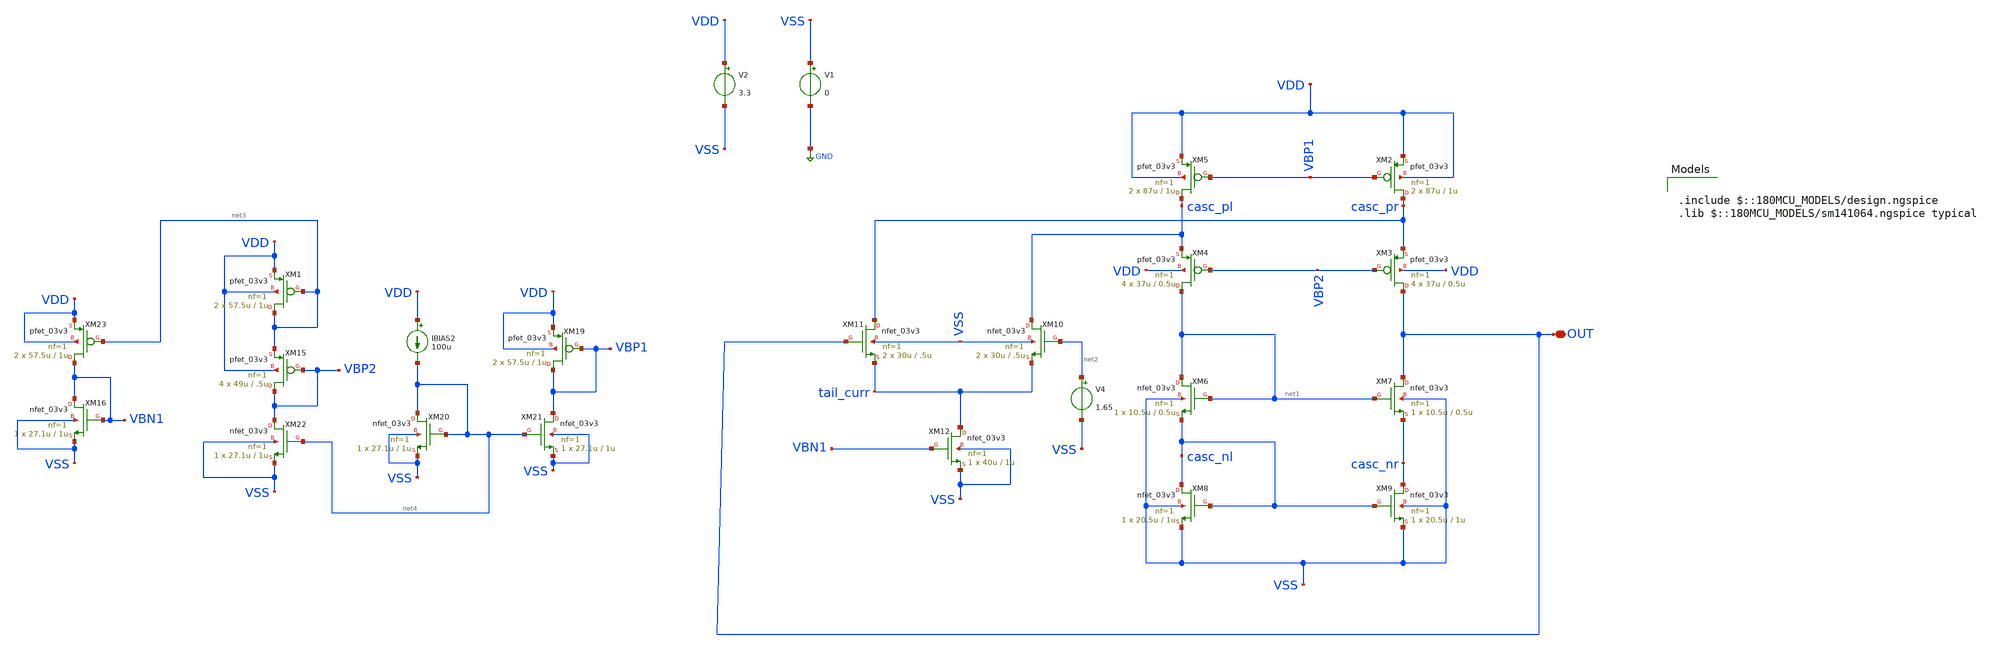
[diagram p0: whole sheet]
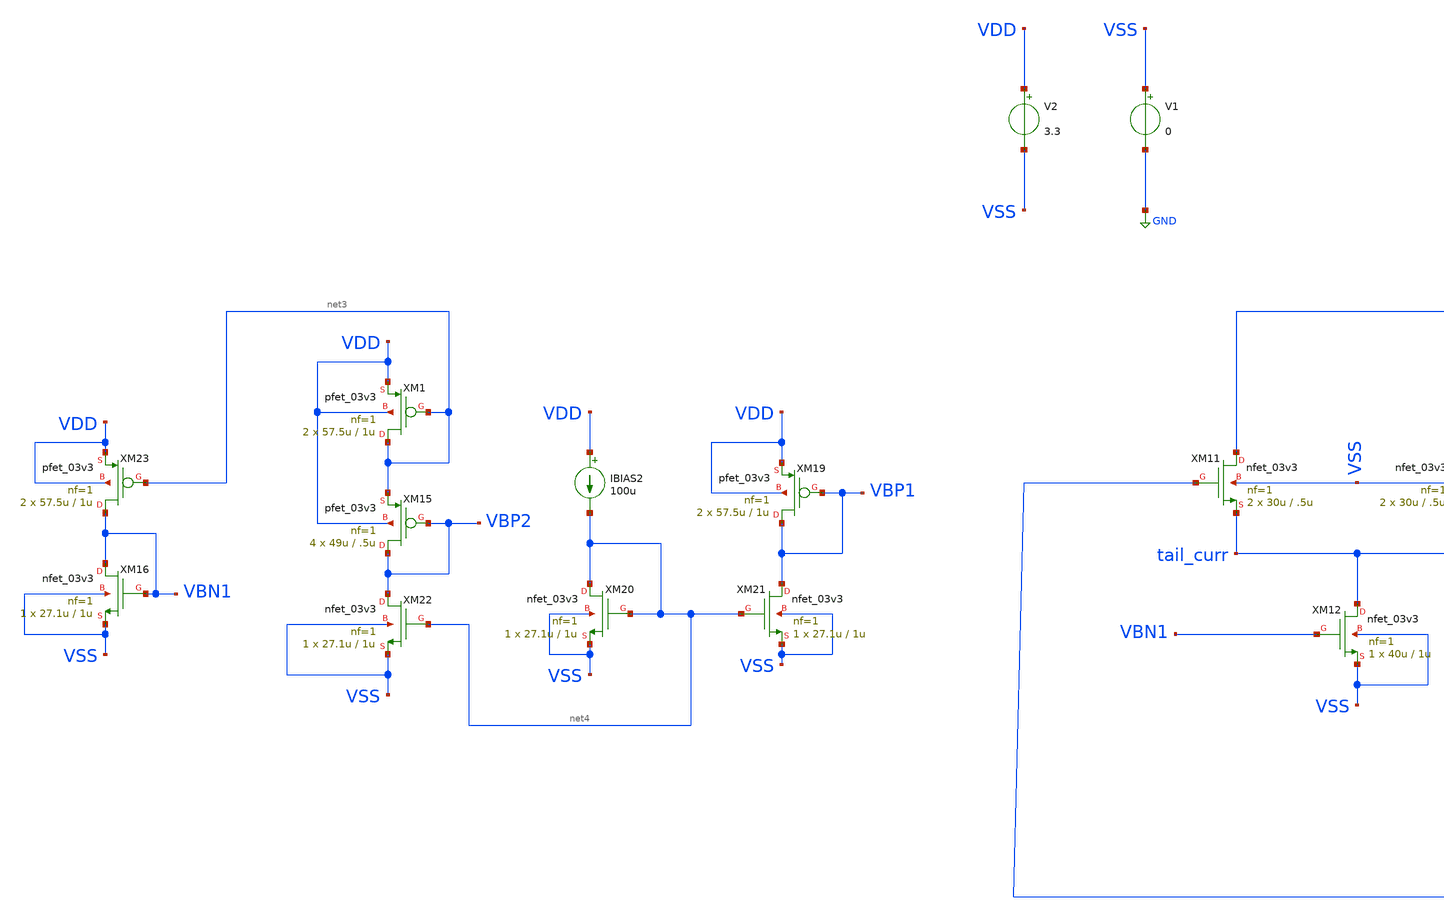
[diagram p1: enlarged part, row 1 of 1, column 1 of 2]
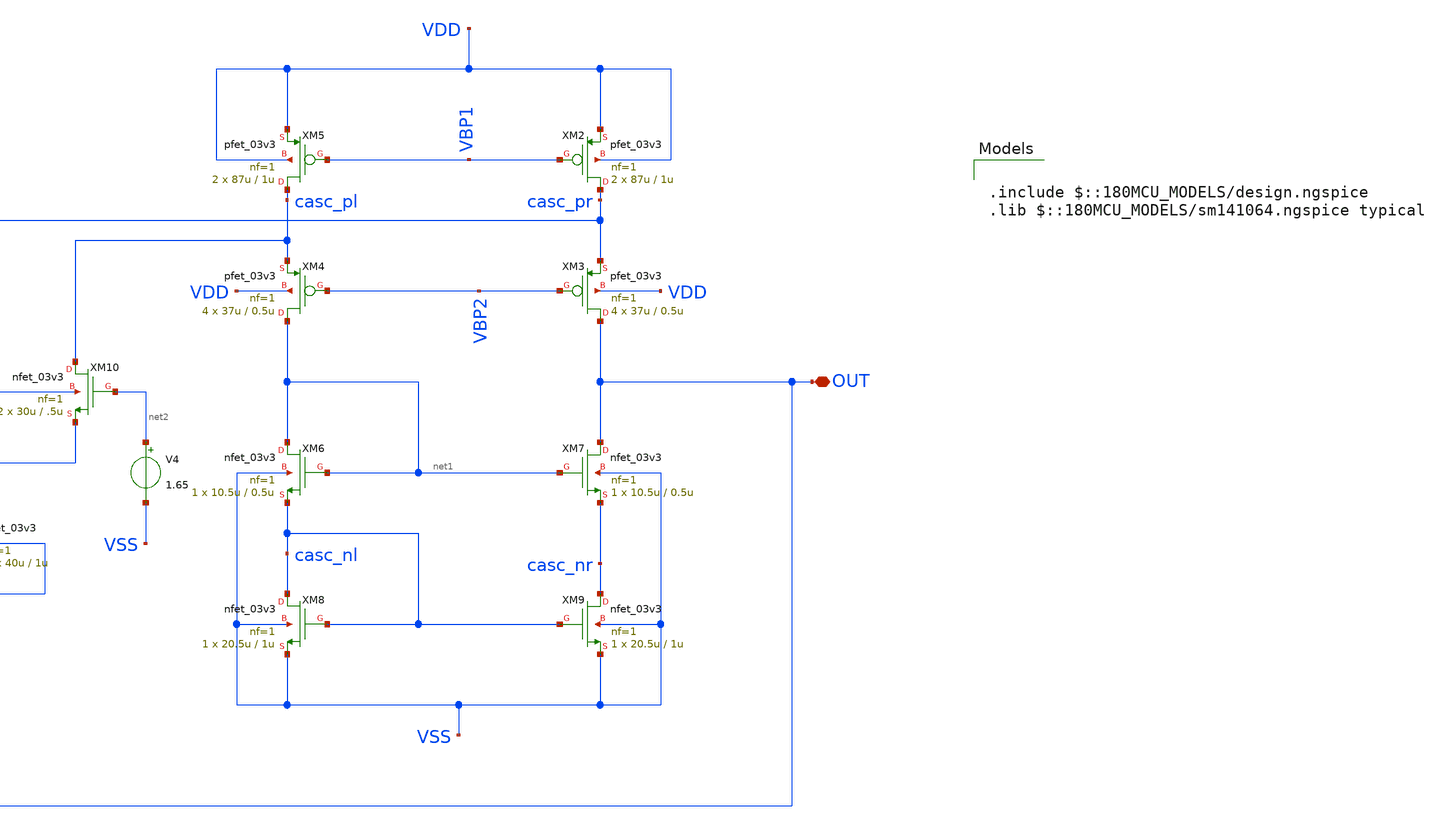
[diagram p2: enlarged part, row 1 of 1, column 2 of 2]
** sch_path: designs/libs/old_files/old_amps/ota_folded_cascode/etj_folded_new_vdsat.sch
**.subckt etj_folded_new_vdsat OUT
*.iopin OUT
XM2 casc_pr VBP1 VDD VDD pfet_03v3 L=1u W=87u nf=1 ad='int((nf+1)/2) * W/nf * 0.18u' as='int((nf+2)/2) * W/nf * 0.18u'
+ pd='2*int((nf+1)/2) * (W/nf + 0.18u)' ps='2*int((nf+2)/2) * (W/nf + 0.18u)' nrd='0.18u / W' nrs='0.18u / W'
+ sa=0 sb=0 sd=0 m=2
XM3 OUT VBP2 casc_pr VDD pfet_03v3 L=0.5u W=37u nf=1 ad='int((nf+1)/2) * W/nf * 0.18u' as='int((nf+2)/2) * W/nf * 0.18u'
+ pd='2*int((nf+1)/2) * (W/nf + 0.18u)' ps='2*int((nf+2)/2) * (W/nf + 0.18u)' nrd='0.18u / W' nrs='0.18u / W'
+ sa=0 sb=0 sd=0 m=4
XM4 net1 VBP2 casc_pl VDD pfet_03v3 L=0.5u W=37u nf=1 ad='int((nf+1)/2) * W/nf * 0.18u' as='int((nf+2)/2) * W/nf * 0.18u'
+ pd='2*int((nf+1)/2) * (W/nf + 0.18u)' ps='2*int((nf+2)/2) * (W/nf + 0.18u)' nrd='0.18u / W' nrs='0.18u / W'
+ sa=0 sb=0 sd=0 m=4
XM5 casc_pl VBP1 VDD VDD pfet_03v3 L=1u W=87u nf=1 ad='int((nf+1)/2) * W/nf * 0.18u' as='int((nf+2)/2) * W/nf * 0.18u'
+ pd='2*int((nf+1)/2) * (W/nf + 0.18u)' ps='2*int((nf+2)/2) * (W/nf + 0.18u)' nrd='0.18u / W' nrs='0.18u / W'
+ sa=0 sb=0 sd=0 m=2
XM6 net1 net1 casc_nl VSS nfet_03v3 L=0.5u W=10.5u nf=1 ad='int((nf+1)/2) * W/nf * 0.18u' as='int((nf+2)/2) * W/nf * 0.18u'
+ pd='2*int((nf+1)/2) * (W/nf + 0.18u)' ps='2*int((nf+2)/2) * (W/nf + 0.18u)' nrd='0.18u / W' nrs='0.18u / W'
+ sa=0 sb=0 sd=0 m=1
XM7 OUT net1 casc_nr VSS nfet_03v3 L=0.5u W=10.5u nf=1 ad='int((nf+1)/2) * W/nf * 0.18u' as='int((nf+2)/2) * W/nf * 0.18u'
+ pd='2*int((nf+1)/2) * (W/nf + 0.18u)' ps='2*int((nf+2)/2) * (W/nf + 0.18u)' nrd='0.18u / W' nrs='0.18u / W'
+ sa=0 sb=0 sd=0 m=1
XM8 casc_nl casc_nl VSS VSS nfet_03v3 L=1u W=20.5u nf=1 ad='int((nf+1)/2) * W/nf * 0.18u' as='int((nf+2)/2) * W/nf * 0.18u'
+ pd='2*int((nf+1)/2) * (W/nf + 0.18u)' ps='2*int((nf+2)/2) * (W/nf + 0.18u)' nrd='0.18u / W' nrs='0.18u / W'
+ sa=0 sb=0 sd=0 m=1
XM9 casc_nr casc_nl VSS VSS nfet_03v3 L=1u W=20.5u nf=1 ad='int((nf+1)/2) * W/nf * 0.18u' as='int((nf+2)/2) * W/nf * 0.18u'
+ pd='2*int((nf+1)/2) * (W/nf + 0.18u)' ps='2*int((nf+2)/2) * (W/nf + 0.18u)' nrd='0.18u / W' nrs='0.18u / W'
+ sa=0 sb=0 sd=0 m=1
XM10 casc_pl net2 tail_curr VSS nfet_03v3 L=.5u W=30u nf=1 ad='int((nf+1)/2) * W/nf * 0.18u' as='int((nf+2)/2) * W/nf * 0.18u'
+ pd='2*int((nf+1)/2) * (W/nf + 0.18u)' ps='2*int((nf+2)/2) * (W/nf + 0.18u)' nrd='0.18u / W' nrs='0.18u / W'
+ sa=0 sb=0 sd=0 m=2
XM12 tail_curr VBN1 VSS VSS nfet_03v3 L=1u W=40u nf=1 ad='int((nf+1)/2) * W/nf * 0.18u' as='int((nf+2)/2) * W/nf * 0.18u'
+ pd='2*int((nf+1)/2) * (W/nf + 0.18u)' ps='2*int((nf+2)/2) * (W/nf + 0.18u)' nrd='0.18u / W' nrs='0.18u / W'
+ sa=0 sb=0 sd=0 m=1
XM11 casc_pr OUT tail_curr VSS nfet_03v3 L=.5u W=30u nf=1 ad='int((nf+1)/2) * W/nf * 0.18u' as='int((nf+2)/2) * W/nf * 0.18u'
+ pd='2*int((nf+1)/2) * (W/nf + 0.18u)' ps='2*int((nf+2)/2) * (W/nf + 0.18u)' nrd='0.18u / W' nrs='0.18u / W'
+ sa=0 sb=0 sd=0 m=2
V2 VDD VSS 3.3
V1 VSS GND 0
V4 net2 VSS 1.65
XM1 net3 net3 VDD VDD pfet_03v3 L=1u W=57.5u nf=1 ad='int((nf+1)/2) * W/nf * 0.18u' as='int((nf+2)/2) * W/nf * 0.18u'
+ pd='2*int((nf+1)/2) * (W/nf + 0.18u)' ps='2*int((nf+2)/2) * (W/nf + 0.18u)' nrd='0.18u / W' nrs='0.18u / W'
+ sa=0 sb=0 sd=0 m=2
XM15 VBP2 VBP2 net3 VDD pfet_03v3 L=.5u W=49u nf=1 ad='int((nf+1)/2) * W/nf * 0.18u' as='int((nf+2)/2) * W/nf * 0.18u'
+ pd='2*int((nf+1)/2) * (W/nf + 0.18u)' ps='2*int((nf+2)/2) * (W/nf + 0.18u)' nrd='0.18u / W' nrs='0.18u / W'
+ sa=0 sb=0 sd=0 m=4
XM16 VBN1 VBN1 VSS VSS nfet_03v3 L=1u W=27.1u nf=1 ad='int((nf+1)/2) * W/nf * 0.18u' as='int((nf+2)/2) * W/nf * 0.18u'
+ pd='2*int((nf+1)/2) * (W/nf + 0.18u)' ps='2*int((nf+2)/2) * (W/nf + 0.18u)' nrd='0.18u / W' nrs='0.18u / W'
+ sa=0 sb=0 sd=0 m=1
XM19 VBP1 VBP1 VDD VDD pfet_03v3 L=1u W=57.5u nf=1 ad='int((nf+1)/2) * W/nf * 0.18u' as='int((nf+2)/2) * W/nf * 0.18u'
+ pd='2*int((nf+1)/2) * (W/nf + 0.18u)' ps='2*int((nf+2)/2) * (W/nf + 0.18u)' nrd='0.18u / W' nrs='0.18u / W'
+ sa=0 sb=0 sd=0 m=2
IBIAS2 VDD net4 100u
XM20 net4 net4 VSS VSS nfet_03v3 L=1u W=27.1u nf=1 ad='int((nf+1)/2) * W/nf * 0.18u' as='int((nf+2)/2) * W/nf * 0.18u'
+ pd='2*int((nf+1)/2) * (W/nf + 0.18u)' ps='2*int((nf+2)/2) * (W/nf + 0.18u)' nrd='0.18u / W' nrs='0.18u / W'
+ sa=0 sb=0 sd=0 m=1
XM21 VBP1 net4 VSS VSS nfet_03v3 L=1u W=27.1u nf=1 ad='int((nf+1)/2) * W/nf * 0.18u' as='int((nf+2)/2) * W/nf * 0.18u'
+ pd='2*int((nf+1)/2) * (W/nf + 0.18u)' ps='2*int((nf+2)/2) * (W/nf + 0.18u)' nrd='0.18u / W' nrs='0.18u / W'
+ sa=0 sb=0 sd=0 m=1
XM22 VBP2 net4 VSS VSS nfet_03v3 L=1u W=27.1u nf=1 ad='int((nf+1)/2) * W/nf * 0.18u' as='int((nf+2)/2) * W/nf * 0.18u'
+ pd='2*int((nf+1)/2) * (W/nf + 0.18u)' ps='2*int((nf+2)/2) * (W/nf + 0.18u)' nrd='0.18u / W' nrs='0.18u / W'
+ sa=0 sb=0 sd=0 m=1
XM23 VBN1 net3 VDD VDD pfet_03v3 L=1u W=57.5u nf=1 ad='int((nf+1)/2) * W/nf * 0.18u' as='int((nf+2)/2) * W/nf * 0.18u'
+ pd='2*int((nf+1)/2) * (W/nf + 0.18u)' ps='2*int((nf+2)/2) * (W/nf + 0.18u)' nrd='0.18u / W' nrs='0.18u / W'
+ sa=0 sb=0 sd=0 m=2
**** begin user architecture code

.include $::180MCU_MODELS/design.ngspice
.lib $::180MCU_MODELS/sm141064.ngspice typical



.control

op

let sat_xm11 = abs(@m.xm11.m0[vds]) - abs(@m.xm11.m0[vdsat])
let sat_xm10 = abs(@m.xm10.m0[vds]) - abs(@m.xm10.m0[vdsat])
let sat_xm12 = abs(@m.xm12.m0[vds]) - abs(@m.xm12.m0[vdsat])
let sat_xm5  = abs(@m.xm5.m0[vds]) - abs(@m.xm5.m0[vdsat])
let sat_xm2  = abs(@m.xm2.m0[vds]) - abs(@m.xm2.m0[vdsat])
let sat_xm4  = abs(@m.xm4.m0[vds]) - abs(@m.xm4.m0[vdsat])
let sat_xm3  = abs(@m.xm3.m0[vds]) - abs(@m.xm3.m0[vdsat])
let sat_xm6  = abs(@m.xm6.m0[vds]) - abs(@m.xm6.m0[vdsat])
let sat_xm7  = abs(@m.xm7.m0[vds]) - abs(@m.xm7.m0[vdsat])
let sat_xm8  = abs(@m.xm8.m0[vds]) - abs(@m.xm8.m0[vdsat])
let sat_xm9  = abs(@m.xm9.m0[vds]) - abs(@m.xm9.m0[vdsat])
let sat_xm19 = abs(@m.xm19.m0[vds]) - abs(@m.xm19.m0[vdsat])
let sat_xm20 = abs(@m.xm20.m0[vds]) - abs(@m.xm20.m0[vdsat])
let sat_xm21 = abs(@m.xm21.m0[vds]) - abs(@m.xm21.m0[vdsat])
let sat_xm22 = abs(@m.xm22.m0[vds]) - abs(@m.xm22.m0[vdsat])
let sat_xm23 = abs(@m.xm23.m0[vds]) - abs(@m.xm23.m0[vdsat])
print sat_xm11 sat_xm10 sat_xm12
print sat_xm5 sat_xm2 sat_xm4 sat_xm3
print sat_xm6 sat_xm7 sat_xm8 sat_xm9
print sat_xm19 sat_xm20 sat_xm21 sat_xm22 sat_xm23

.endc


**** end user architecture code
**.ends
.GLOBAL GND
.end
